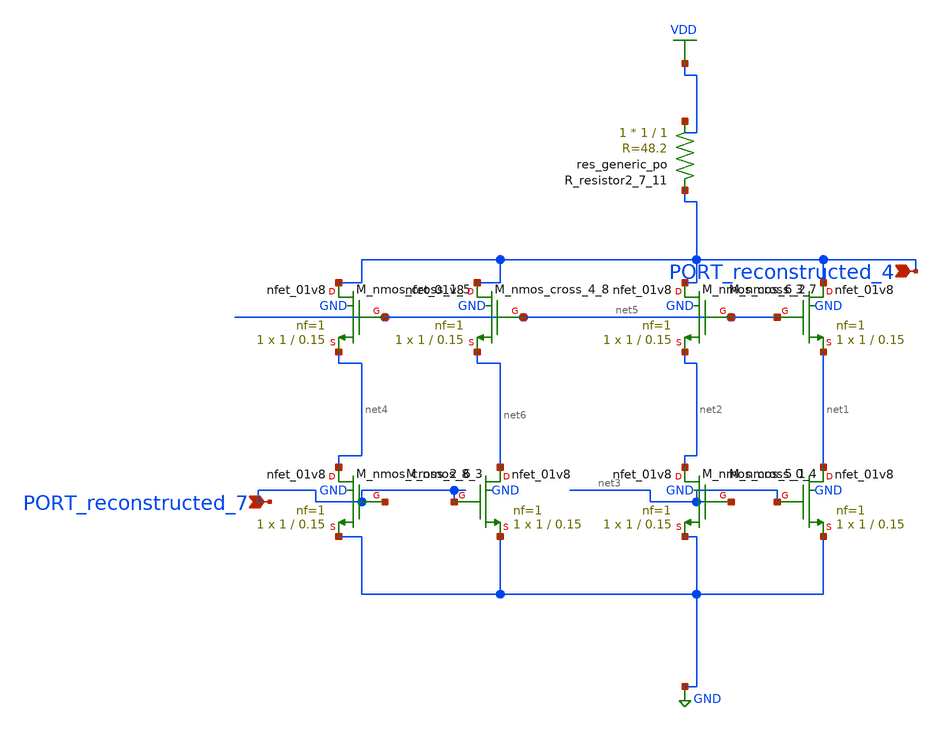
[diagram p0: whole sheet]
** sch_path: schematics/10_1109_IMW48823_2020_9108112_21_001.sch
**.subckt 10_1109_IMW48823_2020_9108112_21_001 PORT_reconstructed_7 PORT_reconstructed_4
*.ipin PORT_reconstructed_7
*.ipin PORT_reconstructed_4
XM_nmos_5_1 net1 net3 GND GND sky130_fd_pr__nfet_01v8 L=0.15 W=1 nf=1 ad='int((1 + 1)/2) * 1 / 1 * 0.29'
+ as='int((1 + 2)/2) * 1 / 1 * 0.29' pd='2*int((1 + 1)/2) * (1 / 1 + 0.29)' ps='2*int((1 + 2)/2) * (1 / 1 + 0.29)'
+ nrd='0.29 / 1 ' nrs='0.29 / 1 ' sa=0 sb=0 sd=0 mult=1 m=1
XM_nmos_6_2 PORT_reconstructed_4 net5 net1 GND sky130_fd_pr__nfet_01v8 L=0.15 W=1 nf=1 ad='int((1 + 1)/2) * 1 / 1 * 0.29'
+ as='int((1 + 2)/2) * 1 / 1 * 0.29' pd='2*int((1 + 1)/2) * (1 / 1 + 0.29)' ps='2*int((1 + 2)/2) * (1 / 1 + 0.29)'
+ nrd='0.29 / 1 ' nrs='0.29 / 1 ' sa=0 sb=0 sd=0 mult=1 m=1
XM_nmos_8_3 net6 PORT_reconstructed_7 GND GND sky130_fd_pr__nfet_01v8 L=0.15 W=1 nf=1 ad='int((1 + 1)/2) * 1 / 1 * 0.29'
+ as='int((1 + 2)/2) * 1 / 1 * 0.29' pd='2*int((1 + 1)/2) * (1 / 1 + 0.29)' ps='2*int((1 + 2)/2) * (1 / 1 + 0.29)'
+ nrd='0.29 / 1 ' nrs='0.29 / 1 ' sa=0 sb=0 sd=0 mult=1 m=1
XM_nmos_cross_0_4 net2 net3 GND GND sky130_fd_pr__nfet_01v8 L=0.15 W=1 nf=1 ad='int((1 + 1)/2) * 1 / 1 * 0.29'
+ as='int((1 + 2)/2) * 1 / 1 * 0.29' pd='2*int((1 + 1)/2) * (1 / 1 + 0.29)' ps='2*int((1 + 2)/2) * (1 / 1 + 0.29)'
+ nrd='0.29 / 1 ' nrs='0.29 / 1 ' sa=0 sb=0 sd=0 mult=1 m=1
XM_nmos_cross_1_5 PORT_reconstructed_4 net5 net4 GND sky130_fd_pr__nfet_01v8 L=0.15 W=1 nf=1 ad='int((1 + 1)/2) * 1 / 1 * 0.29'
+ as='int((1 + 2)/2) * 1 / 1 * 0.29' pd='2*int((1 + 1)/2) * (1 / 1 + 0.29)' ps='2*int((1 + 2)/2) * (1 / 1 + 0.29)'
+ nrd='0.29 / 1 ' nrs='0.29 / 1 ' sa=0 sb=0 sd=0 mult=1 m=1
XM_nmos_cross_2_6 net4 PORT_reconstructed_7 GND GND sky130_fd_pr__nfet_01v8 L=0.15 W=1 nf=1 ad='int((1 + 1)/2) * 1 / 1 * 0.29'
+ as='int((1 + 2)/2) * 1 / 1 * 0.29' pd='2*int((1 + 1)/2) * (1 / 1 + 0.29)' ps='2*int((1 + 2)/2) * (1 / 1 + 0.29)'
+ nrd='0.29 / 1 ' nrs='0.29 / 1 ' sa=0 sb=0 sd=0 mult=1 m=1
XM_nmos_cross_3_7 PORT_reconstructed_4 net5 net2 GND sky130_fd_pr__nfet_01v8 L=0.15 W=1 nf=1 ad='int((1 + 1)/2) * 1 / 1 * 0.29'
+ as='int((1 + 2)/2) * 1 / 1 * 0.29' pd='2*int((1 + 1)/2) * (1 / 1 + 0.29)' ps='2*int((1 + 2)/2) * (1 / 1 + 0.29)'
+ nrd='0.29 / 1 ' nrs='0.29 / 1 ' sa=0 sb=0 sd=0 mult=1 m=1
XM_nmos_cross_4_8 PORT_reconstructed_4 net5 net6 GND sky130_fd_pr__nfet_01v8 L=0.15 W=1 nf=1 ad='int((1 + 1)/2) * 1 / 1 * 0.29'
+ as='int((1 + 2)/2) * 1 / 1 * 0.29' pd='2*int((1 + 1)/2) * (1 / 1 + 0.29)' ps='2*int((1 + 2)/2) * (1 / 1 + 0.29)'
+ nrd='0.29 / 1 ' nrs='0.29 / 1 ' sa=0 sb=0 sd=0 mult=1 m=1
XR_resistor2_7_11 VDD PORT_reconstructed_4 sky130_fd_pr__res_generic_po W=1 L=1 m=1
**.ends
.GLOBAL GND
.GLOBAL VDD
.end
